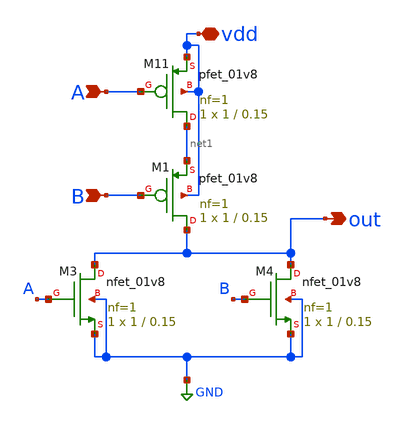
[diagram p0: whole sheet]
** sch_path: designs/subcells/core_nor/nor.sch
**.subckt nor A B vdd out
*.ipin A
*.ipin B
*.iopin vdd
*.opin out
XM3 out A GND GND sky130_fd_pr__nfet_01v8 L=0.15 W=1 nf=1 ad='int((1 + 1)/2) * 1 / 1 * 0.29' as='int((1 + 2)/2) * 1 / 1 * 0.29'
+ pd='2*int((1 + 1)/2) * (1 / 1 + 0.29)' ps='2*int((1 + 2)/2) * (1 / 1 + 0.29)' nrd='0.29 / 1 ' nrs='0.29 / 1 '
+ sa=0 sb=0 sd=0 mult=1 m=1
XM4 out B GND GND sky130_fd_pr__nfet_01v8 L=0.15 W=1 nf=1 ad='int((1 + 1)/2) * 1 / 1 * 0.29' as='int((1 + 2)/2) * 1 / 1 * 0.29'
+ pd='2*int((1 + 1)/2) * (1 / 1 + 0.29)' ps='2*int((1 + 2)/2) * (1 / 1 + 0.29)' nrd='0.29 / 1 ' nrs='0.29 / 1 '
+ sa=0 sb=0 sd=0 mult=1 m=1
XM11 net1 A vdd vdd sky130_fd_pr__pfet_01v8 L=0.15 W=1 nf=1 ad='int((nf+1)/2) * W/nf * 0.29' as='int((nf+2)/2) * W/nf * 0.29'
+ pd='2*int((nf+1)/2) * (W/nf + 0.29)' ps='2*int((nf+2)/2) * (W/nf + 0.29)' nrd='0.29 / W' nrs='0.29 / W'
+ sa=0 sb=0 sd=0 mult=1 m=1
XM1 out B net1 vdd sky130_fd_pr__pfet_01v8 L=0.15 W=1 nf=1 ad='int((nf+1)/2) * W/nf * 0.29' as='int((nf+2)/2) * W/nf * 0.29'
+ pd='2*int((nf+1)/2) * (W/nf + 0.29)' ps='2*int((nf+2)/2) * (W/nf + 0.29)' nrd='0.29 / W' nrs='0.29 / W'
+ sa=0 sb=0 sd=0 mult=1 m=1
**.ends
.GLOBAL GND
.end
